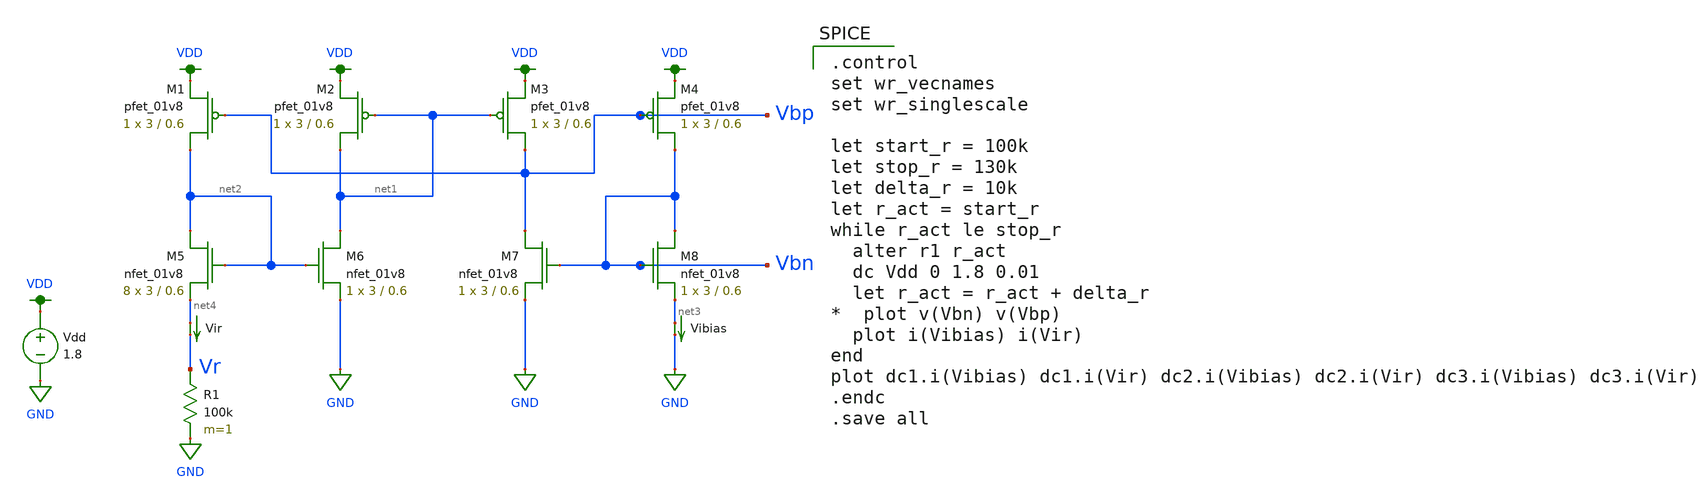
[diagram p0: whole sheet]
** sch_path: mini4/schem/ibias_test_og.sch
**.subckt ibias_test_og
Vdd VDD GND 1.8
R1 Vr GND 100k m=1
XM1 net2 Vbp VDD VDD sky130_fd_pr__pfet_01v8 L=0.6 W=3 nf=1 ad='int((nf+1)/2) * W/nf * 0.29' as='int((nf+2)/2) * W/nf * 0.29'
+ pd='2*int((nf+1)/2) * (W/nf + 0.29)' ps='2*int((nf+2)/2) * (W/nf + 0.29)' nrd='0.29 / W' nrs='0.29 / W'
+ sa=0 sb=0 sd=0 mult=1 m=1
XM2 net1 net1 VDD VDD sky130_fd_pr__pfet_01v8 L=0.6 W=3 nf=1 ad='int((nf+1)/2) * W/nf * 0.29' as='int((nf+2)/2) * W/nf * 0.29'
+ pd='2*int((nf+1)/2) * (W/nf + 0.29)' ps='2*int((nf+2)/2) * (W/nf + 0.29)' nrd='0.29 / W' nrs='0.29 / W'
+ sa=0 sb=0 sd=0 mult=1 m=1
XM3 Vbp net1 VDD VDD sky130_fd_pr__pfet_01v8 L=0.6 W=3 nf=1 ad='int((nf+1)/2) * W/nf * 0.29' as='int((nf+2)/2) * W/nf * 0.29'
+ pd='2*int((nf+1)/2) * (W/nf + 0.29)' ps='2*int((nf+2)/2) * (W/nf + 0.29)' nrd='0.29 / W' nrs='0.29 / W'
+ sa=0 sb=0 sd=0 mult=1 m=1
XM4 Vbn Vbp VDD VDD sky130_fd_pr__pfet_01v8 L=0.6 W=3 nf=1 ad='int((nf+1)/2) * W/nf * 0.29' as='int((nf+2)/2) * W/nf * 0.29'
+ pd='2*int((nf+1)/2) * (W/nf + 0.29)' ps='2*int((nf+2)/2) * (W/nf + 0.29)' nrd='0.29 / W' nrs='0.29 / W'
+ sa=0 sb=0 sd=0 mult=1 m=1
XM5 net2 net2 net4 GND sky130_fd_pr__nfet_01v8 L=0.6 W=3 nf=1 ad='int((nf+1)/2) * W/nf * 0.29' as='int((nf+2)/2) * W/nf * 0.29'
+ pd='2*int((nf+1)/2) * (W/nf + 0.29)' ps='2*int((nf+2)/2) * (W/nf + 0.29)' nrd='0.29 / W' nrs='0.29 / W'
+ sa=0 sb=0 sd=0 mult=8 m=8
XM6 net1 net2 GND GND sky130_fd_pr__nfet_01v8 L=0.6 W=3 nf=1 ad='int((nf+1)/2) * W/nf * 0.29' as='int((nf+2)/2) * W/nf * 0.29'
+ pd='2*int((nf+1)/2) * (W/nf + 0.29)' ps='2*int((nf+2)/2) * (W/nf + 0.29)' nrd='0.29 / W' nrs='0.29 / W'
+ sa=0 sb=0 sd=0 mult=1 m=1
XM7 Vbp Vbn GND GND sky130_fd_pr__nfet_01v8 L=0.6 W=3 nf=1 ad='int((nf+1)/2) * W/nf * 0.29' as='int((nf+2)/2) * W/nf * 0.29'
+ pd='2*int((nf+1)/2) * (W/nf + 0.29)' ps='2*int((nf+2)/2) * (W/nf + 0.29)' nrd='0.29 / W' nrs='0.29 / W'
+ sa=0 sb=0 sd=0 mult=1 m=1
XM8 Vbn Vbn net3 GND sky130_fd_pr__nfet_01v8 L=0.6 W=3 nf=1 ad='int((nf+1)/2) * W/nf * 0.29' as='int((nf+2)/2) * W/nf * 0.29'
+ pd='2*int((nf+1)/2) * (W/nf + 0.29)' ps='2*int((nf+2)/2) * (W/nf + 0.29)' nrd='0.29 / W' nrs='0.29 / W'
+ sa=0 sb=0 sd=0 mult=1 m=1
Vibias net3 GND 0
.save i(vibias)
Vir net4 Vr 0
.save i(vir)
**** begin user architecture code

.option wnflag=1
.param MC_SWITCH=0.0
.lib ~/skywater/skywater-pdk/libraries/sky130_fd_pr_ngspice/latest/models/sky130.lib.spice tt


.control
set wr_vecnames
set wr_singlescale

let start_r = 100k
let stop_r = 130k
let delta_r = 10k
let r_act = start_r
while r_act le stop_r
  alter r1 r_act
  dc Vdd 0 1.8 0.01
  let r_act = r_act + delta_r
*  plot v(Vbn) v(Vbp)
  plot i(Vibias) i(Vir)
end
plot dc1.i(Vibias) dc1.i(Vir) dc2.i(Vibias) dc2.i(Vir) dc3.i(Vibias) dc3.i(Vir)
.endc
.save all


**** end user architecture code
**.ends
.GLOBAL GND
.GLOBAL VDD
.end
